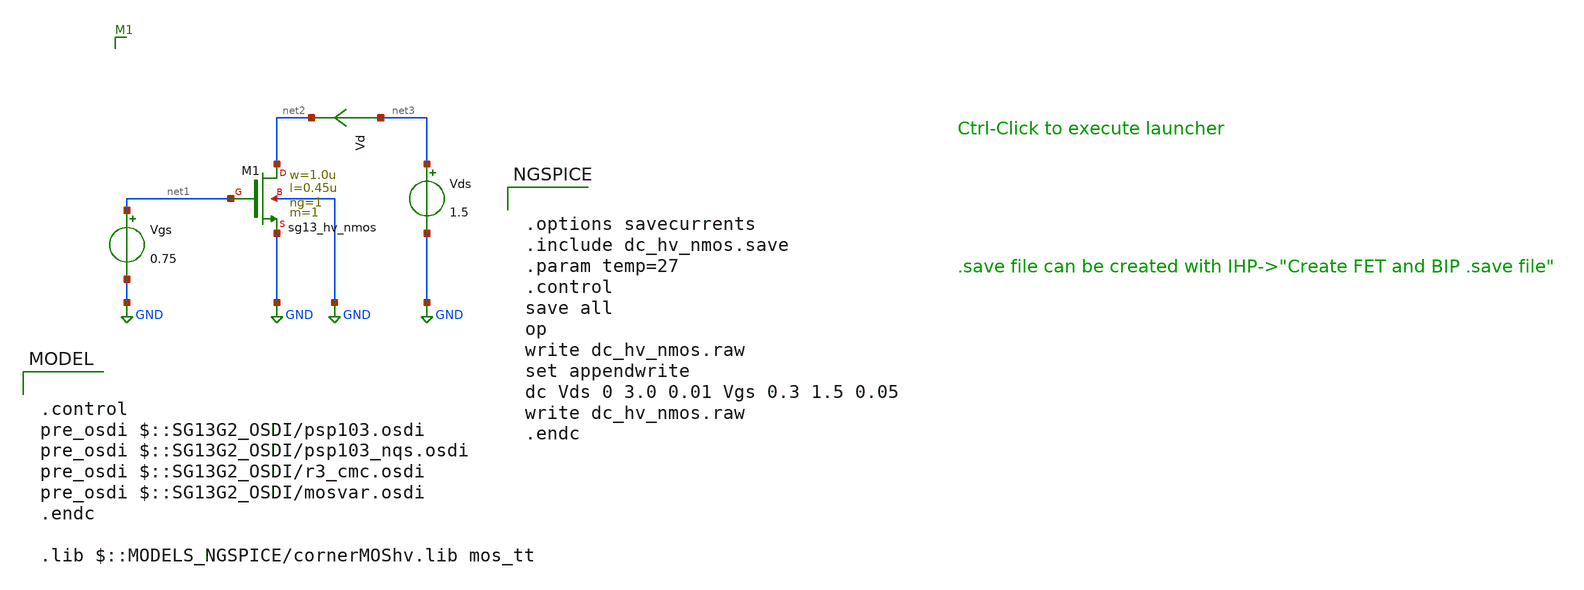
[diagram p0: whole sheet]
** sch_path: ihp-sg13g2/xschem_libs/sg13g2_tests/dc_hv_nmos/schematic/dc_hv_nmos.sch
* Copyright 2023 IHP PDK Authors
**.subckt dc_hv_nmos
Vgs net1 GND 0.75
Vds net3 GND 1.5
Vd net3 net2 0
.save i(vd)
XM1 net2 net1 GND GND sg13_hv_nmos w=1.0u l=0.45u ng=1 m=1 mm_ok=1
**** begin user architecture code

.control
pre_osdi $::SG13G2_OSDI/psp103.osdi
pre_osdi $::SG13G2_OSDI/psp103_nqs.osdi
pre_osdi $::SG13G2_OSDI/r3_cmc.osdi
pre_osdi $::SG13G2_OSDI/mosvar.osdi
.endc

.lib $::MODELS_NGSPICE/cornerMOShv.lib mos_tt



.options savecurrents
.include dc_hv_nmos.save
.param temp=27
.control
save all
op
write dc_hv_nmos.raw
set appendwrite
dc Vds 0 3.0 0.01 Vgs 0.3 1.5 0.05
write dc_hv_nmos.raw
.endc


**** end user architecture code
**.ends
.GLOBAL GND
.end
